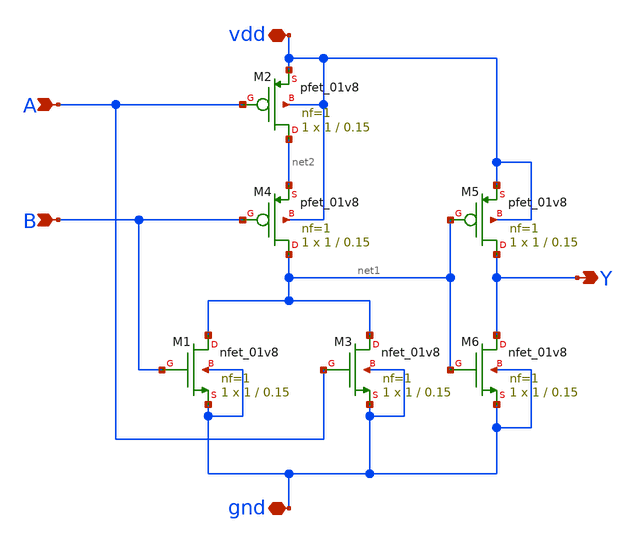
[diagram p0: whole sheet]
** sch_path: Primitives/OR Gate/Xschem Files/sky130_orgate.sch
**.subckt sky130_orgate A B gnd vdd Y
*.ipin A
*.ipin B
*.iopin gnd
*.iopin vdd
*.opin Y
XM1 net1 B gnd gnd sky130_fd_pr__nfet_01v8 L=0.15 W=1 nf=1 ad='int((1 + 1)/2) * 1 / 1 * 0.29' as='int((1 + 2)/2) * 1 / 1 * 0.29'
+ pd='2*int((1 + 1)/2) * (1 / 1 + 0.29)' ps='2*int((1 + 2)/2) * (1 / 1 + 0.29)' nrd='0.29 / 1 ' nrs='0.29 / 1 '
+ sa=0 sb=0 sd=0 mult=1 m=1
XM2 net2 A vdd vdd sky130_fd_pr__pfet_01v8 L=0.15 W=1 nf=1 ad='int((1 + 1)/2) * 1 / 1 * 0.29' as='int((1 + 2)/2) * 1 / 1 * 0.29'
+ pd='2*int((1 + 1)/2) * (1 / 1 + 0.29)' ps='2*int((1 + 2)/2) * (1 / 1 + 0.29)' nrd='0.29 / 1 ' nrs='0.29 / 1 '
+ sa=0 sb=0 sd=0 mult=1 m=1
XM3 net1 A gnd gnd sky130_fd_pr__nfet_01v8 L=0.15 W=1 nf=1 ad='int((1 + 1)/2) * 1 / 1 * 0.29' as='int((1 + 2)/2) * 1 / 1 * 0.29'
+ pd='2*int((1 + 1)/2) * (1 / 1 + 0.29)' ps='2*int((1 + 2)/2) * (1 / 1 + 0.29)' nrd='0.29 / 1 ' nrs='0.29 / 1 '
+ sa=0 sb=0 sd=0 mult=1 m=1
XM4 net1 B net2 vdd sky130_fd_pr__pfet_01v8 L=0.15 W=1 nf=1 ad='int((1 + 1)/2) * 1 / 1 * 0.29' as='int((1 + 2)/2) * 1 / 1 * 0.29'
+ pd='2*int((1 + 1)/2) * (1 / 1 + 0.29)' ps='2*int((1 + 2)/2) * (1 / 1 + 0.29)' nrd='0.29 / 1 ' nrs='0.29 / 1 '
+ sa=0 sb=0 sd=0 mult=1 m=1
XM5 Y net1 vdd vdd sky130_fd_pr__pfet_01v8 L=0.15 W=1 nf=1 ad='int((1 + 1)/2) * 1 / 1 * 0.29' as='int((1 + 2)/2) * 1 / 1 * 0.29'
+ pd='2*int((1 + 1)/2) * (1 / 1 + 0.29)' ps='2*int((1 + 2)/2) * (1 / 1 + 0.29)' nrd='0.29 / 1 ' nrs='0.29 / 1 '
+ sa=0 sb=0 sd=0 mult=1 m=1
XM6 Y net1 gnd gnd sky130_fd_pr__nfet_01v8 L=0.15 W=1 nf=1 ad='int((1 + 1)/2) * 1 / 1 * 0.29' as='int((1 + 2)/2) * 1 / 1 * 0.29'
+ pd='2*int((1 + 1)/2) * (1 / 1 + 0.29)' ps='2*int((1 + 2)/2) * (1 / 1 + 0.29)' nrd='0.29 / 1 ' nrs='0.29 / 1 '
+ sa=0 sb=0 sd=0 mult=1 m=1
**.ends
.end
